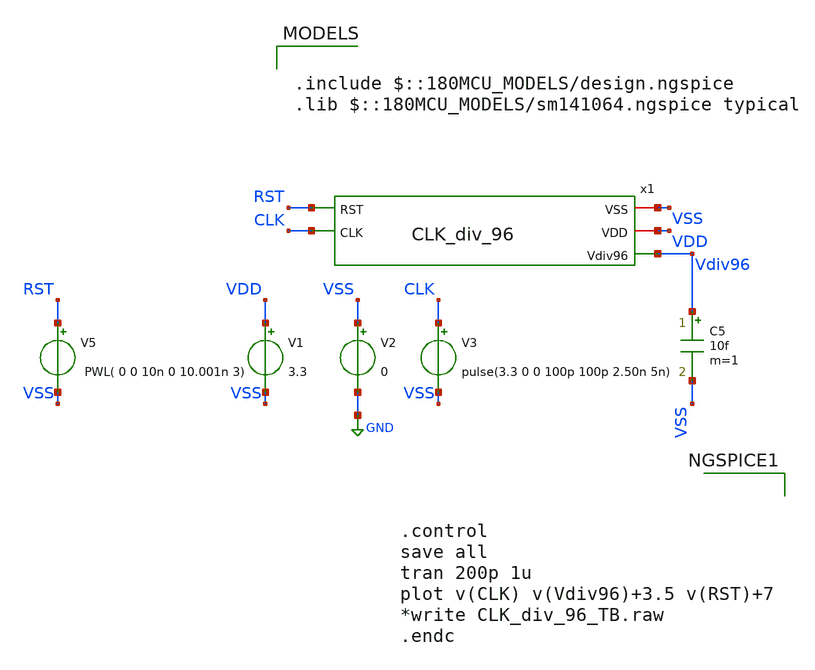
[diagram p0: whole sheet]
** sch_path: Clock_Generator_PAKISTAN_02/xschem/CLK_div_96_TB.sch
**.subckt CLK_div_96_TB
V1 VDD VSS 3.3
V2 VSS GND 0
V3 CLK VSS pulse(3.3 0 0 100p 100p 2.50n 5n)
C5 Vdiv96 VSS 10f m=1
V5 RST VSS PWL( 0 0 10n 0 10.001n 3)
x1 VSS VDD RST Vdiv96 CLK CLK_div_96
**** begin user architecture code

.include $::180MCU_MODELS/design.ngspice
.lib $::180MCU_MODELS/sm141064.ngspice typical




.control
save all
tran 200p 1u
plot v(CLK) v(Vdiv96)+3.5 v(RST)+7
*write CLK_div_96_TB.raw
.endc


**** end user architecture code
**.ends
.GLOBAL GND
.end
